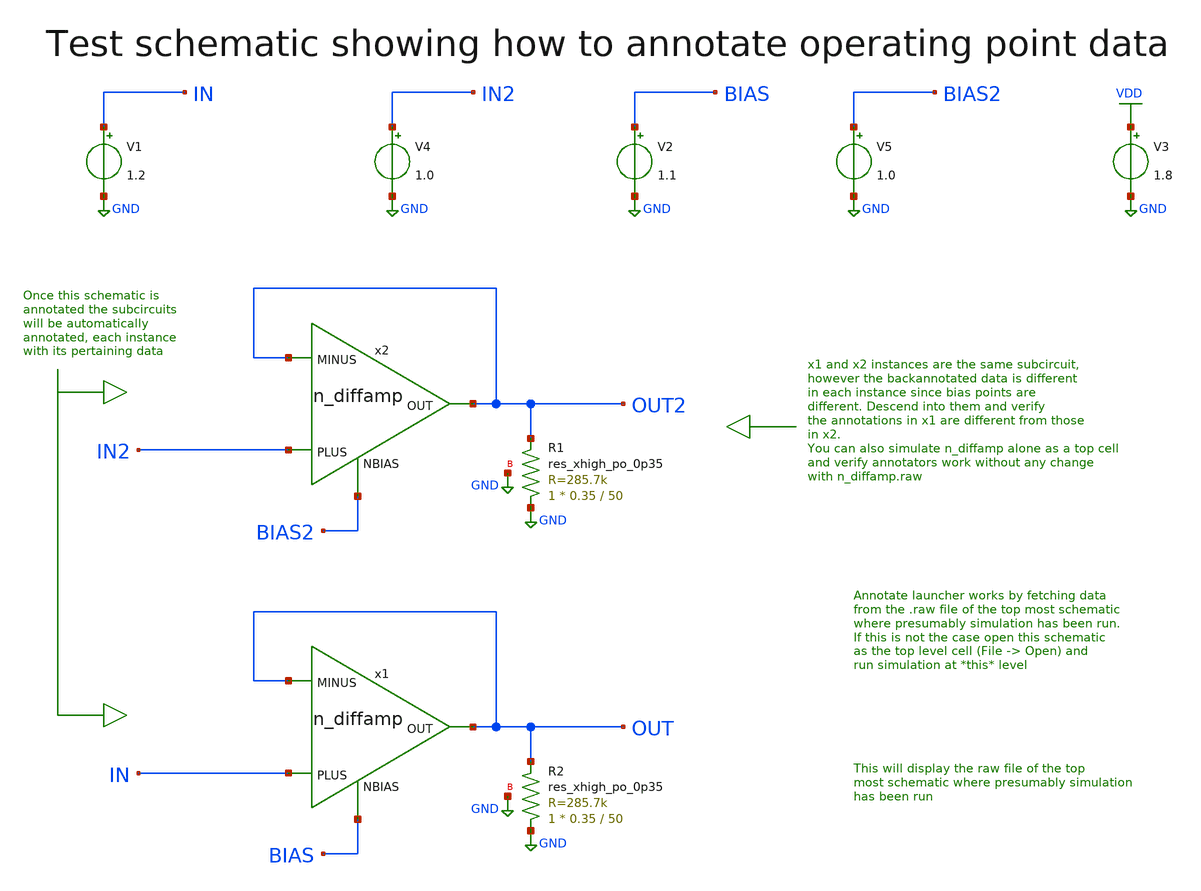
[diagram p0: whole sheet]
** sch_path: sky130_tests/test_analog.sch
* Copyright 2021 Stefan Frederik Schippers
* Licensed under the Apache License, Version 2.0 (the "License");
* you may not use this file except in compliance with the License.
* You may obtain a copy of the License at
* https://www.apache.org/licenses/LICENSE-2.0
* Unless required by applicable law or agreed to in writing, software
* distributed under the License is distributed on an "AS IS" BASIS,
* WITHOUT WARRANTIES OR CONDITIONS OF ANY KIND, either express or implied.
* See the License for the specific language governing permissions and
* limitations under the License.
**.subckt test_analog
x1 OUT OUT IN BIAS n_diffamp
x2 OUT2 OUT2 IN2 BIAS2 n_diffamp
V1 IN GND 1.2
V2 BIAS GND 1.1
V3 VDD GND 1.8
V4 IN2 GND 1.0
V5 BIAS2 GND 1.0
XR1 GND OUT2 GND sky130_fd_pr__res_xhigh_po_0p35 L=50 mult=1 m=1
XR2 GND OUT GND sky130_fd_pr__res_xhigh_po_0p35 L=50 mult=1 m=1
**** begin user architecture code

** opencircuitdesign pdks install
.lib $::SKYWATER_MODELS/sky130.lib.spice tt

**** end user architecture code
**.ends

* expanding   symbol:  sky130_tests/n_diffamp.sym # of pins=4
** sym_path: sky130_tests/n_diffamp.sym
** sch_path: sky130_tests/n_diffamp.sch
.subckt n_diffamp OUT MINUS PLUS NBIAS
*.ipin PLUS
*.ipin MINUS
*.opin OUT
*.ipin NBIAS
XM1 net1 PLUS S GND sky130_fd_pr__nfet_01v8_lvt L=0.3 W=2 nf=1 ad='int((1 + 1)/2) * 2 / 1 * 0.29' as='int((1 + 2)/2) * 2 / 1 * 0.29'
+ pd='2*int((1 + 1)/2) * (2 / 1 + 0.29)' ps='2*int((1 + 2)/2) * (2 / 1 + 0.29)' nrd='0.29 / 2 ' nrs='0.29 / 2 '
+ sa=0 sb=0 sd=0 mult=1 m=1
XM2 OUT MINUS S GND sky130_fd_pr__nfet_01v8_lvt L=0.3 W=2 nf=1 ad='int((1 + 1)/2) * 2 / 1 * 0.29' as='int((1 + 2)/2) * 2 / 1 * 0.29'
+ pd='2*int((1 + 1)/2) * (2 / 1 + 0.29)' ps='2*int((1 + 2)/2) * (2 / 1 + 0.29)' nrd='0.29 / 2 ' nrs='0.29 / 2 '
+ sa=0 sb=0 sd=0 mult=1 m=1
XM3 OUT net1 VDD VDD sky130_fd_pr__pfet_01v8_lvt L=0.8 W=4 nf=1 ad='int((1 + 1)/2) * 4 / 1 * 0.29' as='int((1 + 2)/2) * 4 / 1 * 0.29'
+ pd='2*int((1 + 1)/2) * (4 / 1 + 0.29)' ps='2*int((1 + 2)/2) * (4 / 1 + 0.29)' nrd='0.29 / 4 ' nrs='0.29 / 4 '
+ sa=0 sb=0 sd=0 mult=1 m=1
XM4 net1 net1 VDD VDD sky130_fd_pr__pfet_01v8_lvt L=0.8 W=4 nf=1 ad='int((1 + 1)/2) * 4 / 1 * 0.29' as='int((1 + 2)/2) * 4 / 1 * 0.29'
+ pd='2*int((1 + 1)/2) * (4 / 1 + 0.29)' ps='2*int((1 + 2)/2) * (4 / 1 + 0.29)' nrd='0.29 / 4 ' nrs='0.29 / 4 '
+ sa=0 sb=0 sd=0 mult=1 m=1
XM5 net2 NBIAS GND GND sky130_fd_pr__nfet_01v8 L=1.2 W=0.7 nf=1 ad='int((1 + 1)/2) * 0.7 / 1 * 0.29'
+ as='int((1 + 2)/2) * 0.7 / 1 * 0.29' pd='2*int((1 + 1)/2) * (0.7 / 1 + 0.29)' ps='2*int((1 + 2)/2) * (0.7 / 1 + 0.29)'
+ nrd='0.29 / 0.7 ' nrs='0.29 / 0.7 ' sa=0 sb=0 sd=0 mult=1 m=1
XR1 GND S GND sky130_fd_pr__res_xhigh_po_0p35 L=50 mult=1 m=1
V5 S net2 0
.save i(v5)
.ends

.GLOBAL GND
.GLOBAL VDD
**** begin user architecture code


* ngspice commands
.options savecurrents
.include test_analog.save
.control
save all
op
print @m.x2.xm5.msky130_fd_pr__nfet_01v8[vth]
write test_analog.raw
* quit 0
.endc



**** end user architecture code
.end
